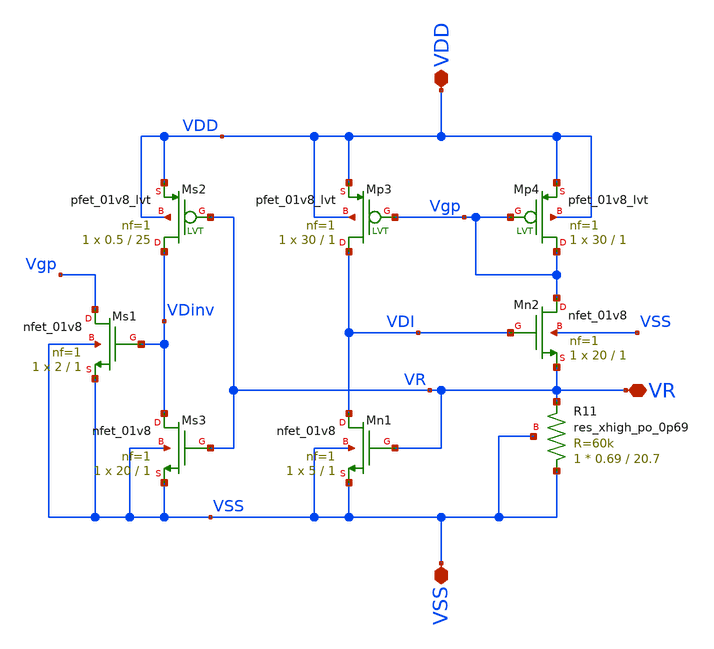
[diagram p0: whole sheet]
** sch_path: xschem/Iref/self_bias.sch
**.subckt self_bias VR VDD VSS
*.iopin VR
*.iopin VDD
*.iopin VSS
XMp4 Vgp Vgp VDD VDD sky130_fd_pr__pfet_01v8_lvt L=1 W=30 nf=1 ad='int((1 + 1)/2) * 30 / 1 * 0.29' as='int((1 + 2)/2) * 30 / 1 * 0.29'
+ pd='2*int((1 + 1)/2) * (30 / 1 + 0.29)' ps='2*int((1 + 2)/2) * (30 / 1 + 0.29)' nrd='0.29 / 30 ' nrs='0.29 / 30 '
+ sa=0 sb=0 sd=0 mult=1 m=1
XMp3 VDI Vgp VDD VDD sky130_fd_pr__pfet_01v8_lvt L=1 W=30 nf=1 ad='int((1 + 1)/2) * 30 / 1 * 0.29' as='int((1 + 2)/2) * 30 / 1 * 0.29'
+ pd='2*int((1 + 1)/2) * (30 / 1 + 0.29)' ps='2*int((1 + 2)/2) * (30 / 1 + 0.29)' nrd='0.29 / 30 ' nrs='0.29 / 30 '
+ sa=0 sb=0 sd=0 mult=1 m=1
XMs2 VDinv VR VDD VDD sky130_fd_pr__pfet_01v8_lvt L=25 W=0.5 nf=1 ad='int((1 + 1)/2) * 0.5 / 1 * 0.29'
+ as='int((1 + 2)/2) * 0.5 / 1 * 0.29' pd='2*int((1 + 1)/2) * (0.5 / 1 + 0.29)' ps='2*int((1 + 2)/2) * (0.5 / 1 + 0.29)'
+ nrd='0.29 / 0.5 ' nrs='0.29 / 0.5 ' sa=0 sb=0 sd=0 mult=1 m=1
XMn2 Vgp VDI VR VSS sky130_fd_pr__nfet_01v8 L=1 W=20 nf=1 ad='int((1 + 1)/2) * 20 / 1 * 0.29' as='int((1 + 2)/2) * 20 / 1 * 0.29'
+ pd='2*int((1 + 1)/2) * (20 / 1 + 0.29)' ps='2*int((1 + 2)/2) * (20 / 1 + 0.29)' nrd='0.29 / 20 ' nrs='0.29 / 20 '
+ sa=0 sb=0 sd=0 mult=1 m=1
XMn1 VDI VR VSS VSS sky130_fd_pr__nfet_01v8 L=1 W=5 nf=1 ad='int((1 + 1)/2) * 5 / 1 * 0.29' as='int((1 + 2)/2) * 5 / 1 * 0.29'
+ pd='2*int((1 + 1)/2) * (5 / 1 + 0.29)' ps='2*int((1 + 2)/2) * (5 / 1 + 0.29)' nrd='0.29 / 5 ' nrs='0.29 / 5 '
+ sa=0 sb=0 sd=0 mult=1 m=1
XMs3 VDinv VR VSS VSS sky130_fd_pr__nfet_01v8 L=1 W=20 nf=1 ad='int((1 + 1)/2) * 20 / 1 * 0.29' as='int((1 + 2)/2) * 20 / 1 * 0.29'
+ pd='2*int((1 + 1)/2) * (20 / 1 + 0.29)' ps='2*int((1 + 2)/2) * (20 / 1 + 0.29)' nrd='0.29 / 20 ' nrs='0.29 / 20 '
+ sa=0 sb=0 sd=0 mult=1 m=1
XMs1 Vgp VDinv VSS VSS sky130_fd_pr__nfet_01v8 L=1 W=2 nf=1 ad='int((1 + 1)/2) * 2 / 1 * 0.29' as='int((1 + 2)/2) * 2 / 1 * 0.29'
+ pd='2*int((1 + 1)/2) * (2 / 1 + 0.29)' ps='2*int((1 + 2)/2) * (2 / 1 + 0.29)' nrd='0.29 / 2 ' nrs='0.29 / 2 '
+ sa=0 sb=0 sd=0 mult=1 m=1
XR11 VSS VR VSS sky130_fd_pr__res_xhigh_po_0p69 L=20.7 mult=1 m=1
**.ends
.end
